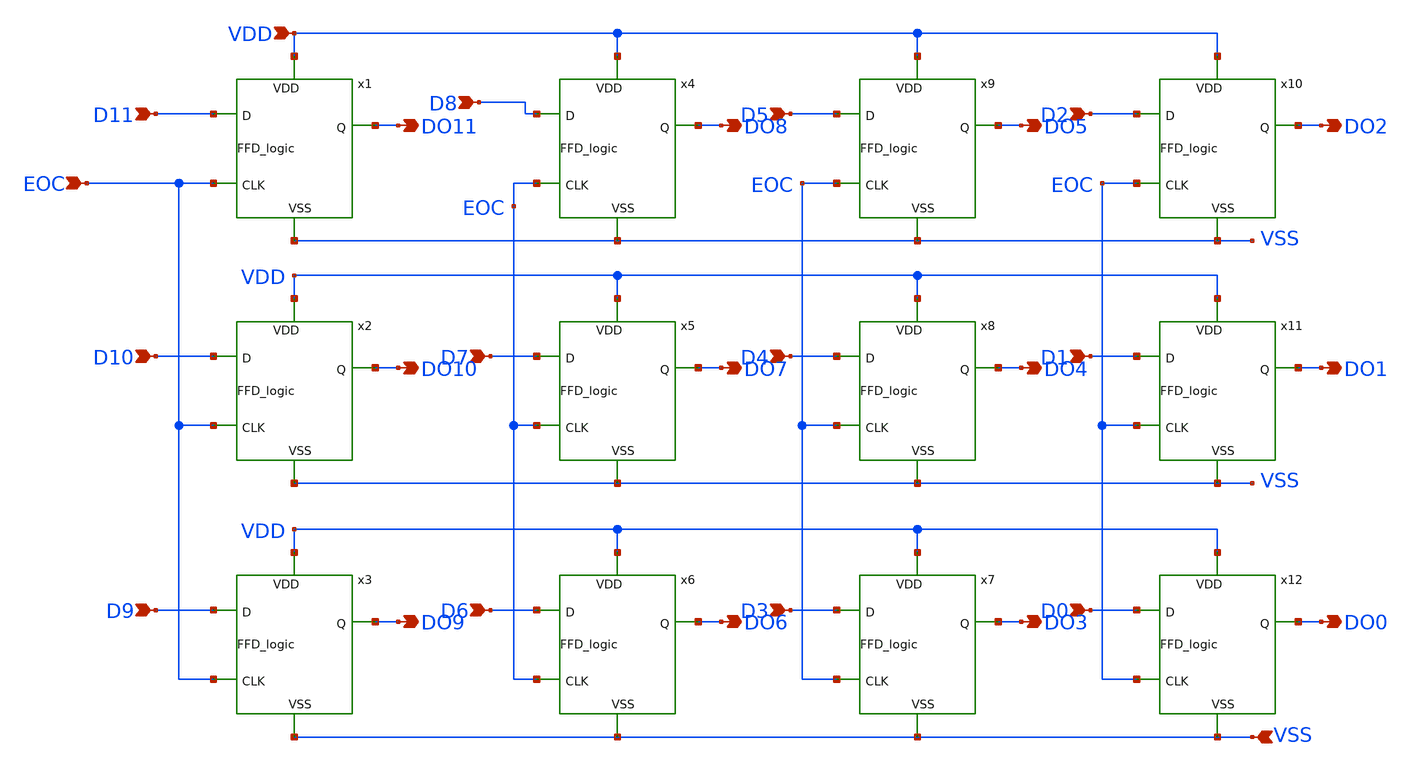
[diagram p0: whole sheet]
** sch_path: SAR_Register_v2.sch
**.subckt SAR_Register_v2 VDD VSS D11 D10 D9 D8 D7 D6 D5 D4 D3 D2 D1 D0 DO11 DO10 DO9 DO8 DO7 DO6
*+ DO3 DO4 DO5 DO2 DO1 DO0 EOC
*.ipin VDD
*.ipin VSS
*.ipin D11
*.ipin D10
*.ipin D9
*.ipin D8
*.ipin D7
*.ipin D6
*.ipin D5
*.ipin D4
*.ipin D3
*.ipin D2
*.ipin D1
*.ipin D0
*.opin DO11
*.opin DO10
*.opin DO9
*.opin DO8
*.opin DO7
*.opin DO6
*.opin DO3
*.opin DO4
*.opin DO5
*.opin DO2
*.opin DO1
*.opin DO0
*.ipin EOC
x1 DO11 D11 VDD EOC VSS FFD_logic
x2 DO10 D10 VDD EOC VSS FFD_logic
x3 DO9 D9 VDD EOC VSS FFD_logic
x4 DO8 D8 VDD EOC VSS FFD_logic
x5 DO7 D7 VDD EOC VSS FFD_logic
x6 DO6 D6 VDD EOC VSS FFD_logic
x7 DO3 D3 VDD EOC VSS FFD_logic
x8 DO4 D4 VDD EOC VSS FFD_logic
x9 DO5 D5 VDD EOC VSS FFD_logic
x10 DO2 D2 VDD EOC VSS FFD_logic
x11 DO1 D1 VDD EOC VSS FFD_logic
x12 DO0 D0 VDD EOC VSS FFD_logic
**.ends

* expanding   symbol:  FFD_logic.sym # of pins=5
** sym_path: FFD_logic.sym
** sch_path: FFD_logic.sch
.subckt FFD_logic Q D VDD CLK VSS
*.ipin D
*.ipin CLK
*.ipin VDD
*.ipin VSS
*.opin Q
x1 VDD net3 D net2 VSS nand_FFD
x2 VDD net4 net2 net1 VSS nand_FFD
x3 VDD net5 net3 net6 VSS nand_FFD
x4 VDD net6 net5 net4 VSS nand_FFD
x5 VDD net8 net5 CLK VSS nand_FFD
x6 VDD net7 CLK net6 VSS nand_FFD
x7 VDD Q net8 net9 VSS nand_FFD
x8 VDD net9 Q net7 VSS nand_FFD
x9 VDD D net1 VSS Inverter
x10 VDD CLK net2 VSS Inverter
.ends


* expanding   symbol:  nand_FFD.sym # of pins=5
** sym_path: nand_FFD.sym
** sch_path: nand_FFD.sch
.subckt nand_FFD VDD Y A B VSS
*.ipin VDD
*.ipin A
*.ipin B
*.ipin VSS
*.opin Y
XM1 Y A net1 VSS sky130_fd_pr__nfet_01v8 L=0.15 W=1 nf=1 ad='int((nf+1)/2) * W/nf * 0.29' as='int((nf+2)/2) * W/nf * 0.29'
+ pd='2*int((nf+1)/2) * (W/nf + 0.29)' ps='2*int((nf+2)/2) * (W/nf + 0.29)' nrd='0.29 / W' nrs='0.29 / W'
+ sa=0 sb=0 sd=0 mult=1 m=1
XM2 net1 B VSS VSS sky130_fd_pr__nfet_01v8 L=0.15 W=1 nf=1 ad='int((nf+1)/2) * W/nf * 0.29' as='int((nf+2)/2) * W/nf * 0.29'
+ pd='2*int((nf+1)/2) * (W/nf + 0.29)' ps='2*int((nf+2)/2) * (W/nf + 0.29)' nrd='0.29 / W' nrs='0.29 / W'
+ sa=0 sb=0 sd=0 mult=1 m=1
XM3 Y A VDD VDD sky130_fd_pr__pfet_01v8 L=0.15 W=2 nf=1 ad='int((nf+1)/2) * W/nf * 0.29' as='int((nf+2)/2) * W/nf * 0.29'
+ pd='2*int((nf+1)/2) * (W/nf + 0.29)' ps='2*int((nf+2)/2) * (W/nf + 0.29)' nrd='0.29 / W' nrs='0.29 / W'
+ sa=0 sb=0 sd=0 mult=1 m=1
XM4 Y B VDD VDD sky130_fd_pr__pfet_01v8 L=0.15 W=2 nf=1 ad='int((nf+1)/2) * W/nf * 0.29' as='int((nf+2)/2) * W/nf * 0.29'
+ pd='2*int((nf+1)/2) * (W/nf + 0.29)' ps='2*int((nf+2)/2) * (W/nf + 0.29)' nrd='0.29 / W' nrs='0.29 / W'
+ sa=0 sb=0 sd=0 mult=1 m=1
.ends


* expanding   symbol:  Inverter.sym # of pins=4
** sym_path: Inverter.sym
** sch_path: Inverter.sch
.subckt Inverter VDD IN OUT VSS
*.ipin IN
*.ipin VSS
*.ipin VDD
*.opin OUT
XM1 OUT IN VSS VSS sky130_fd_pr__nfet_01v8 L=0.3 W=1 nf=1 ad='int((nf+1)/2) * W/nf * 0.29' as='int((nf+2)/2) * W/nf * 0.29'
+ pd='2*int((nf+1)/2) * (W/nf + 0.29)' ps='2*int((nf+2)/2) * (W/nf + 0.29)' nrd='0.29 / W' nrs='0.29 / W'
+ sa=0 sb=0 sd=0 mult=1 m=1
XM2 OUT IN VDD VDD sky130_fd_pr__pfet_01v8 L=0.3 W=2 nf=1 ad='int((nf+1)/2) * W/nf * 0.29' as='int((nf+2)/2) * W/nf * 0.29'
+ pd='2*int((nf+1)/2) * (W/nf + 0.29)' ps='2*int((nf+2)/2) * (W/nf + 0.29)' nrd='0.29 / W' nrs='0.29 / W'
+ sa=0 sb=0 sd=0 mult=1 m=1
.ends

.end
